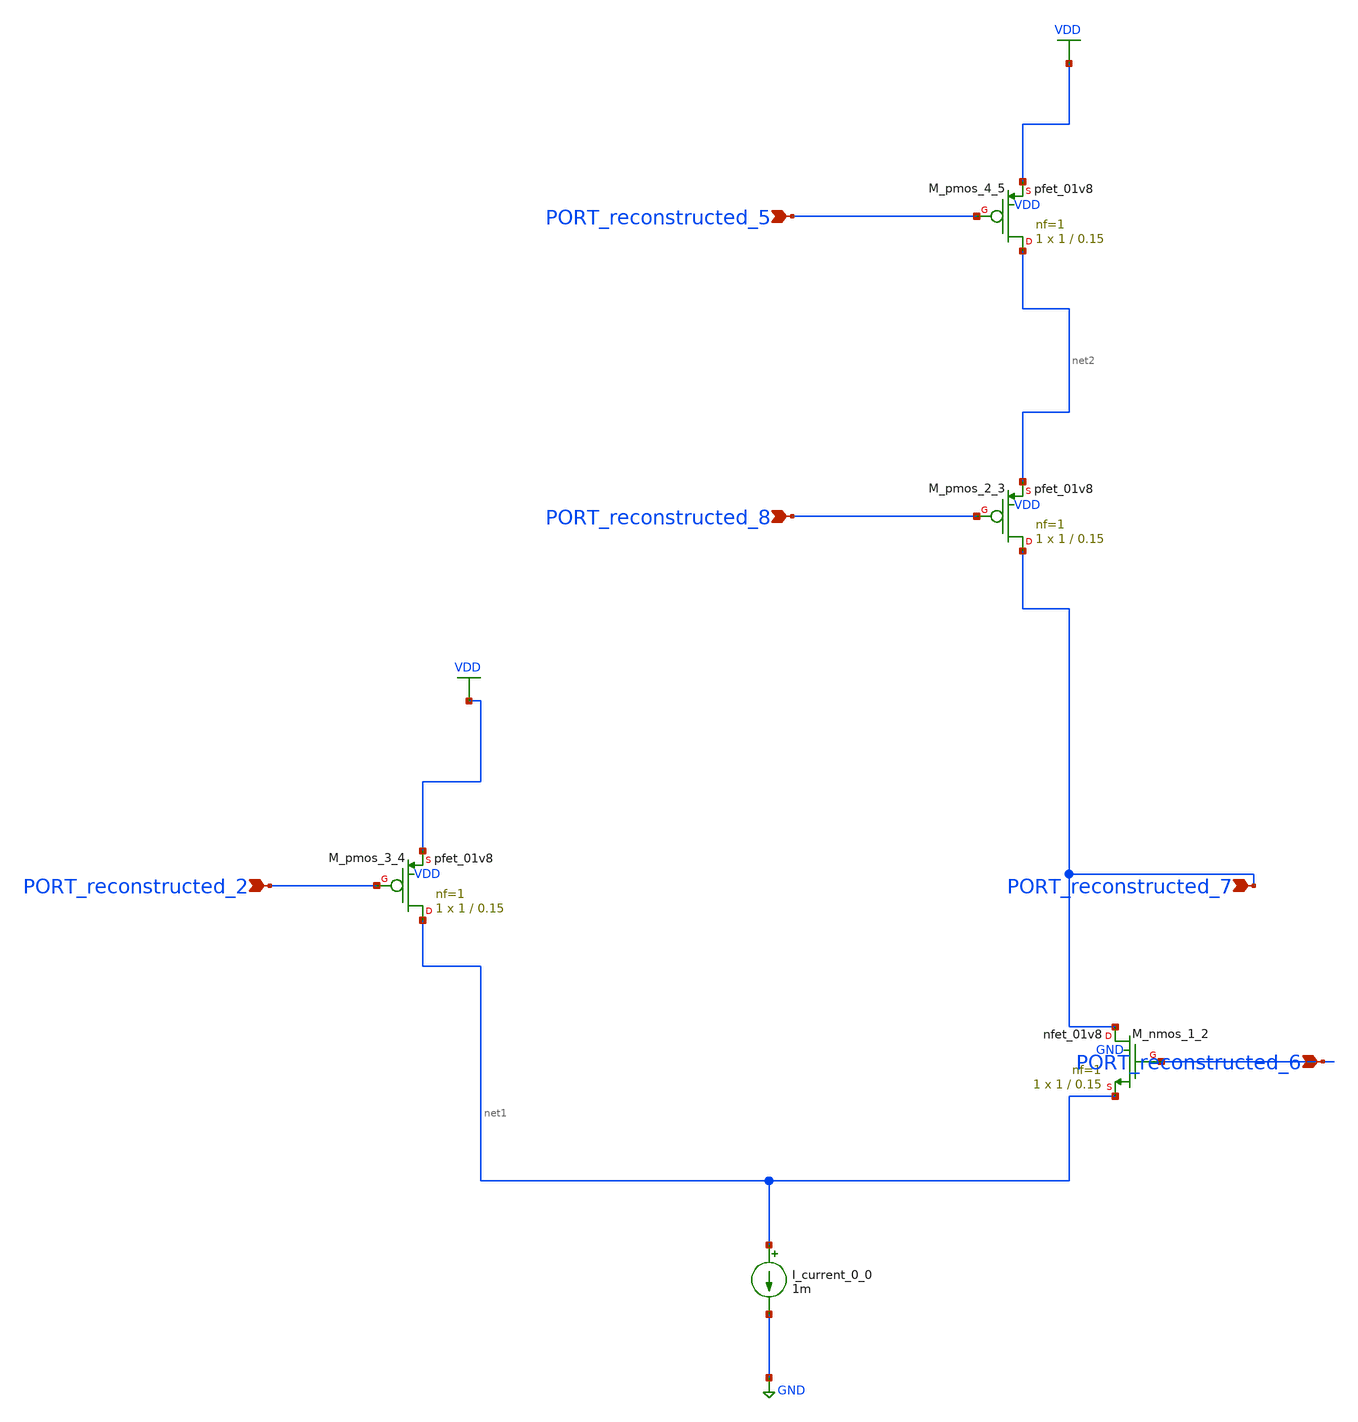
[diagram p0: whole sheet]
** sch_path: schematics/AMSNet/145.sch
**.subckt 145 PORT_reconstructed_5 PORT_reconstructed_6 PORT_reconstructed_7 PORT_reconstructed_2
*+ PORT_reconstructed_8
*.ipin PORT_reconstructed_5
*.ipin PORT_reconstructed_6
*.ipin PORT_reconstructed_7
*.ipin PORT_reconstructed_2
*.ipin PORT_reconstructed_8
I_current_0_0 net1 GND 1m
XM_nmos_1_2 PORT_reconstructed_7 PORT_reconstructed_6 net1 GND sky130_fd_pr__nfet_01v8 L=0.15 W=1 nf=1
+ ad='int((1 + 1)/2) * 1 / 1 * 0.29' as='int((1 + 2)/2) * 1 / 1 * 0.29' pd='2*int((1 + 1)/2) * (1 / 1 + 0.29)'
+ ps='2*int((1 + 2)/2) * (1 / 1 + 0.29)' nrd='0.29 / 1 ' nrs='0.29 / 1 ' sa=0 sb=0 sd=0 mult=1 m=1
XM_pmos_2_3 PORT_reconstructed_7 PORT_reconstructed_8 net2 VDD sky130_fd_pr__pfet_01v8 L=0.15 W=1 nf=1
+ ad='int((1 + 1)/2) * 1 / 1 * 0.29' as='int((1 + 2)/2) * 1 / 1 * 0.29' pd='2*int((1 + 1)/2) * (1 / 1 + 0.29)'
+ ps='2*int((1 + 2)/2) * (1 / 1 + 0.29)' nrd='0.29 / 1 ' nrs='0.29 / 1 ' sa=0 sb=0 sd=0 mult=1 m=1
XM_pmos_3_4 net1 PORT_reconstructed_2 VDD VDD sky130_fd_pr__pfet_01v8 L=0.15 W=1 nf=1 ad='int((1 + 1)/2) * 1 / 1 * 0.29'
+ as='int((1 + 2)/2) * 1 / 1 * 0.29' pd='2*int((1 + 1)/2) * (1 / 1 + 0.29)' ps='2*int((1 + 2)/2) * (1 / 1 + 0.29)'
+ nrd='0.29 / 1 ' nrs='0.29 / 1 ' sa=0 sb=0 sd=0 mult=1 m=1
XM_pmos_4_5 net2 PORT_reconstructed_5 VDD VDD sky130_fd_pr__pfet_01v8 L=0.15 W=1 nf=1 ad='int((1 + 1)/2) * 1 / 1 * 0.29'
+ as='int((1 + 2)/2) * 1 / 1 * 0.29' pd='2*int((1 + 1)/2) * (1 / 1 + 0.29)' ps='2*int((1 + 2)/2) * (1 / 1 + 0.29)'
+ nrd='0.29 / 1 ' nrs='0.29 / 1 ' sa=0 sb=0 sd=0 mult=1 m=1
**.ends
.GLOBAL GND
.GLOBAL VDD
.end
